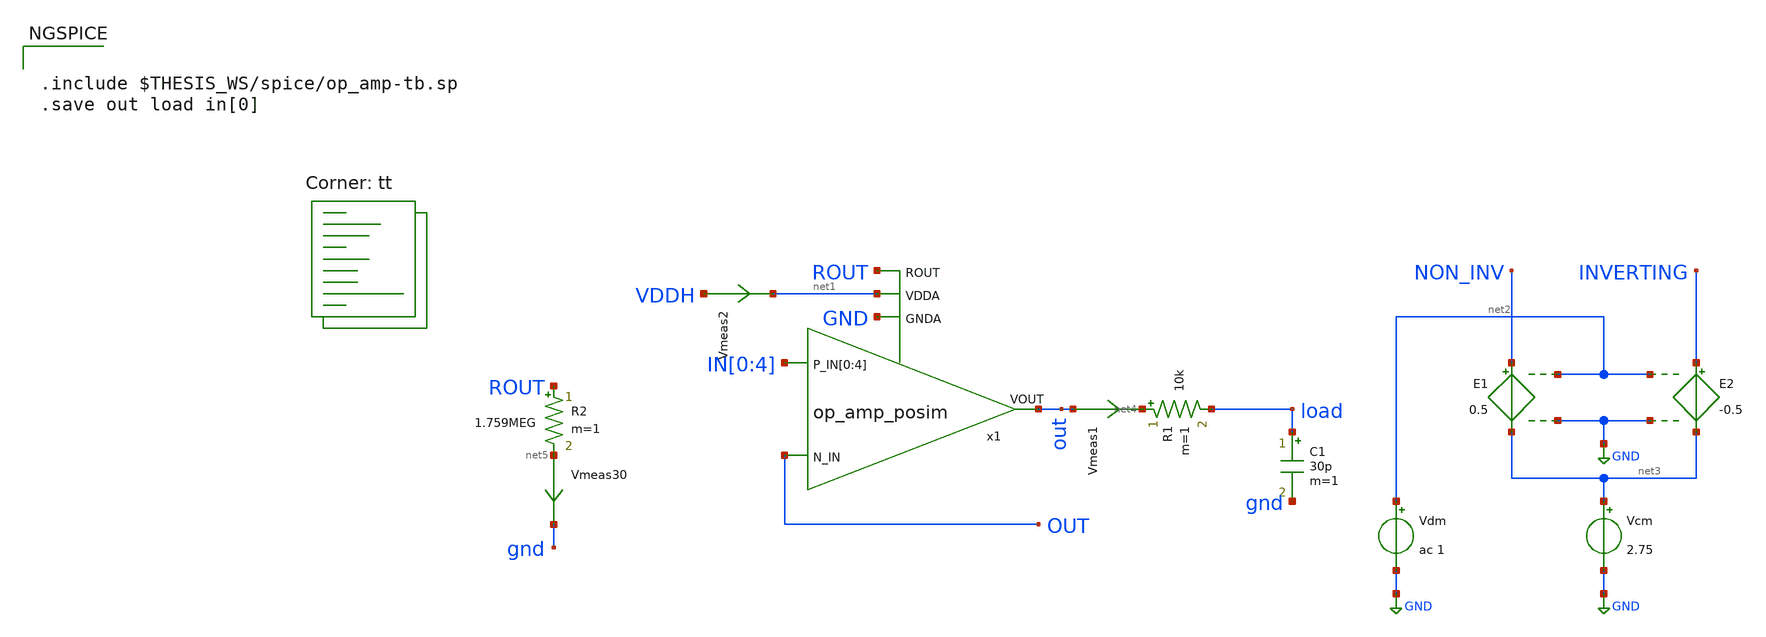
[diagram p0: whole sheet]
** sch_path: xschem/op_amp_top-tb.sch
**.subckt op_amp_top-tb
C1 load gnd 30p m=1
R1 net4 load 10k m=1
Vmeas1 out net4 0
.save i(vmeas1)
Vmeas30 net5 gnd 0
.save i(vmeas30)
Vmeas2 VDDH net1 0
.save i(vmeas2)
E1 NON_INV net3 net2 GND 0.5
E2 INVERTING net3 net2 GND -0.5
Vdm net2 GND ac 1
Vcm net3 GND 2.75
x1 IN[0] IN[1] IN[2] IN[3] IN[4] OUT out ROUT net1 GND op_amp_posim
R2 ROUT net5 1.759MEG m=1
**** begin user architecture code


.include $THESIS_WS/spice/op_amp-tb.sp
.save out load in[0]


.lib $::SKYWATER_MODELS/sky130.lib.spice tt
**** end user architecture code
**.ends
.GLOBAL GND
.end
